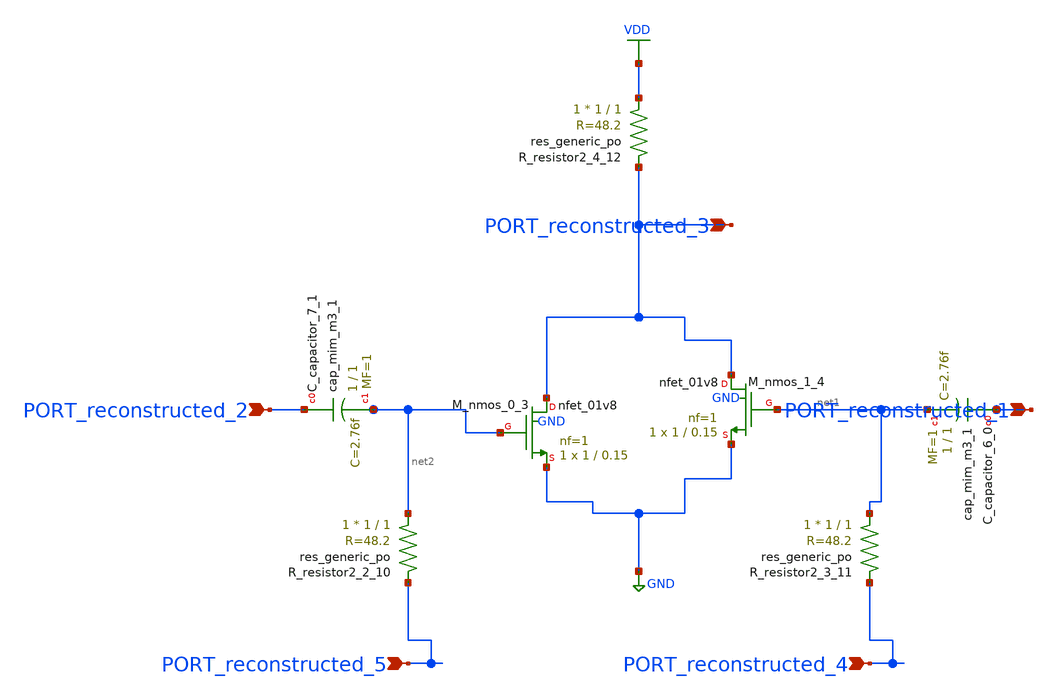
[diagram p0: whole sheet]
** sch_path: schematics/SchemGen/10_1109_ACCESS_2021_3064007_05_003.sch
**.subckt 10_1109_ACCESS_2021_3064007_05_003 PORT_reconstructed_2 PORT_reconstructed_1
*+ PORT_reconstructed_3 PORT_reconstructed_4 PORT_reconstructed_5
*.ipin PORT_reconstructed_2
*.ipin PORT_reconstructed_1
*.ipin PORT_reconstructed_3
*.ipin PORT_reconstructed_4
*.ipin PORT_reconstructed_5
XC_capacitor_6_0 PORT_reconstructed_1 net1 sky130_fd_pr__cap_mim_m3_1 W=1 L=1 MF=1 m=1
XC_capacitor_7_1 PORT_reconstructed_2 net2 sky130_fd_pr__cap_mim_m3_1 W=1 L=1 MF=1 m=1
XM_nmos_0_3 PORT_reconstructed_3 net2 GND GND sky130_fd_pr__nfet_01v8 L=0.15 W=1 nf=1 ad='int((1 + 1)/2) * 1 / 1 * 0.29'
+ as='int((1 + 2)/2) * 1 / 1 * 0.29' pd='2*int((1 + 1)/2) * (1 / 1 + 0.29)' ps='2*int((1 + 2)/2) * (1 / 1 + 0.29)'
+ nrd='0.29 / 1 ' nrs='0.29 / 1 ' sa=0 sb=0 sd=0 mult=1 m=1
XM_nmos_1_4 PORT_reconstructed_3 net1 GND GND sky130_fd_pr__nfet_01v8 L=0.15 W=1 nf=1 ad='int((1 + 1)/2) * 1 / 1 * 0.29'
+ as='int((1 + 2)/2) * 1 / 1 * 0.29' pd='2*int((1 + 1)/2) * (1 / 1 + 0.29)' ps='2*int((1 + 2)/2) * (1 / 1 + 0.29)'
+ nrd='0.29 / 1 ' nrs='0.29 / 1 ' sa=0 sb=0 sd=0 mult=1 m=1
XR_resistor2_2_10 net2 PORT_reconstructed_5 sky130_fd_pr__res_generic_po W=1 L=1 m=1
XR_resistor2_3_11 net1 PORT_reconstructed_4 sky130_fd_pr__res_generic_po W=1 L=1 m=1
XR_resistor2_4_12 VDD PORT_reconstructed_3 sky130_fd_pr__res_generic_po W=1 L=1 m=1
**.ends
.GLOBAL GND
.GLOBAL VDD
.end
